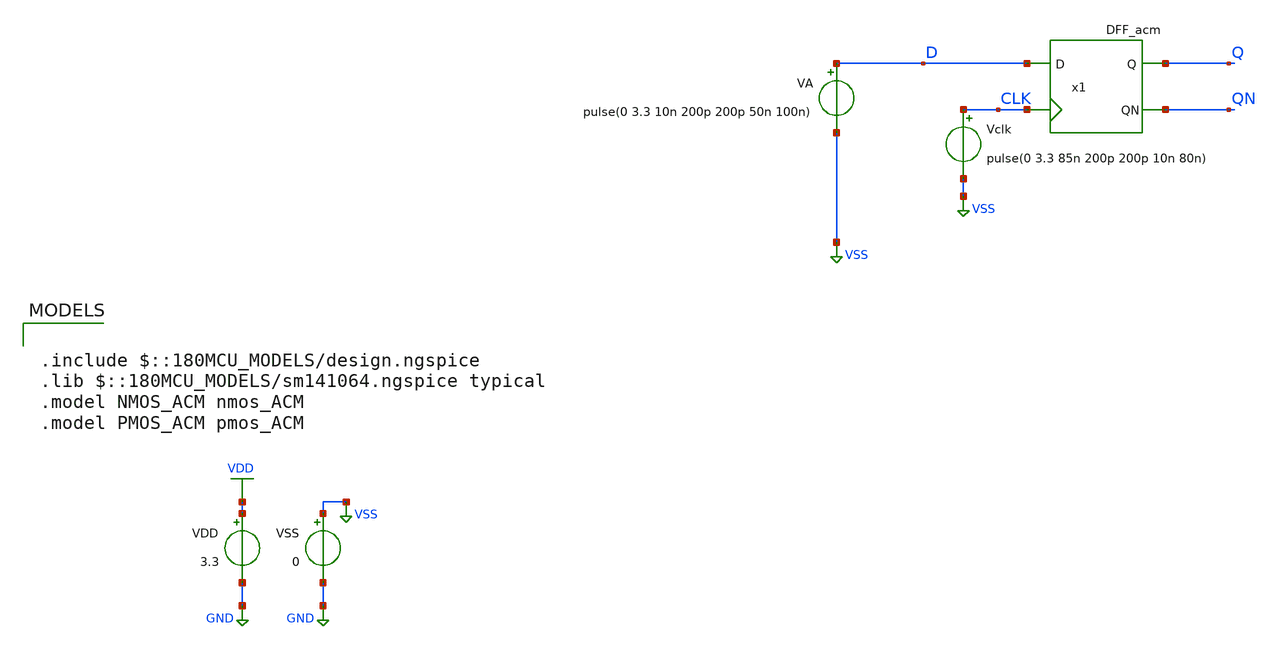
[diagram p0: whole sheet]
** sch_path: legacy/Examples/GF180MCU/xschem/TB_DFF_acm.sch
**.subckt TB_DFF_acm
VA D VSS pulse(0 3.3 10n 200p 200p 50n 100n)
Vclk CLK VSS pulse(0 3.3 85n 200p 200p 10n 80n)
x1 Q QN D CLK VDD VSS DFF_acm
VDD VDD GND 3.3
VSS VSS GND 0
**** begin user architecture code

.include $::180MCU_MODELS/design.ngspice
.lib $::180MCU_MODELS/sm141064.ngspice typical
.model NMOS_ACM nmos_ACM
.model PMOS_ACM pmos_ACM



.option gmin=1e-15
.control
pre_osdi ./NMOS_ACM_2V0.osdi
pre_osdi ./PMOS_ACM_2V0.osdi
save all


tran 0.1n 500n
remzerovec
write TB_DFF_acm.raw
set appendwrite

.endc


**** end user architecture code
**.ends
.GLOBAL GND
.GLOBAL VDD
.GLOBAL VSS
.end
